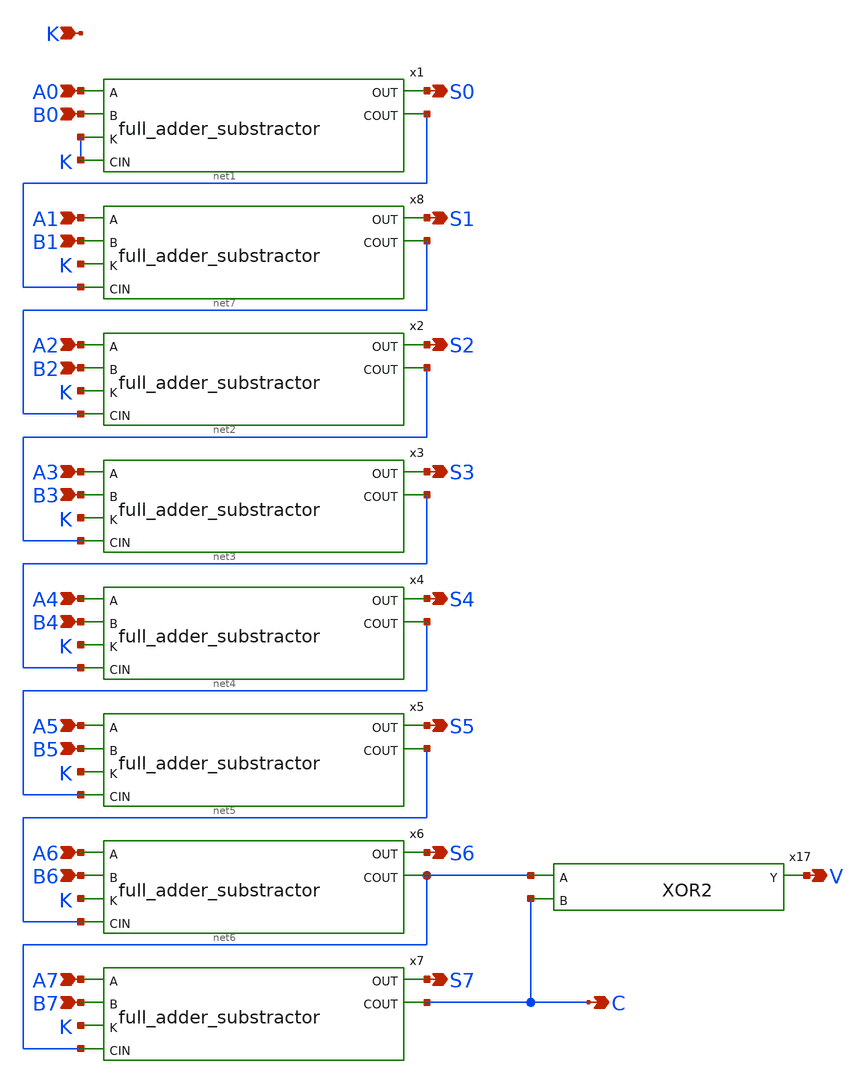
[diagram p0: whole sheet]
** sch_path: design/xschem/ADDER/8-bit_adder_subtractor.sch
**.subckt 8-bit_adder_subtractor A0 B0 S0 K A1 B1 S1 A2 B2 S2 A3 B3 S3 A4 B4 S4 A5 B5 S5 A6 B6 S6 A7
*+ B7 S7 C V
*.ipin A0
*.ipin B0
*.opin S0
*.ipin K
*.ipin A1
*.ipin B1
*.opin S1
*.ipin A2
*.ipin B2
*.opin S2
*.ipin A3
*.ipin B3
*.opin S3
*.ipin A4
*.ipin B4
*.opin S4
*.ipin A5
*.ipin B5
*.opin S5
*.ipin A6
*.ipin B6
*.opin S6
*.ipin A7
*.ipin B7
*.opin S7
*.opin C
*.opin V
x17 net6 C V VSS VDD XOR2
x1 A0 K B0 K S0 net1 VSS VDD full_adder_substractor
x2 A2 K B2 net7 S2 net2 VSS VDD full_adder_substractor
x3 A3 K B3 net2 S3 net3 VSS VDD full_adder_substractor
x4 A4 K B4 net3 S4 net4 VSS VDD full_adder_substractor
x5 A5 K B5 net4 S5 net5 VSS VDD full_adder_substractor
x6 A6 K B6 net5 S6 net6 VSS VDD full_adder_substractor
x7 A7 K B7 net6 S7 C VSS VDD full_adder_substractor
x8 A1 K B1 net1 S1 net7 VSS VDD full_adder_substractor
**.ends
.end
